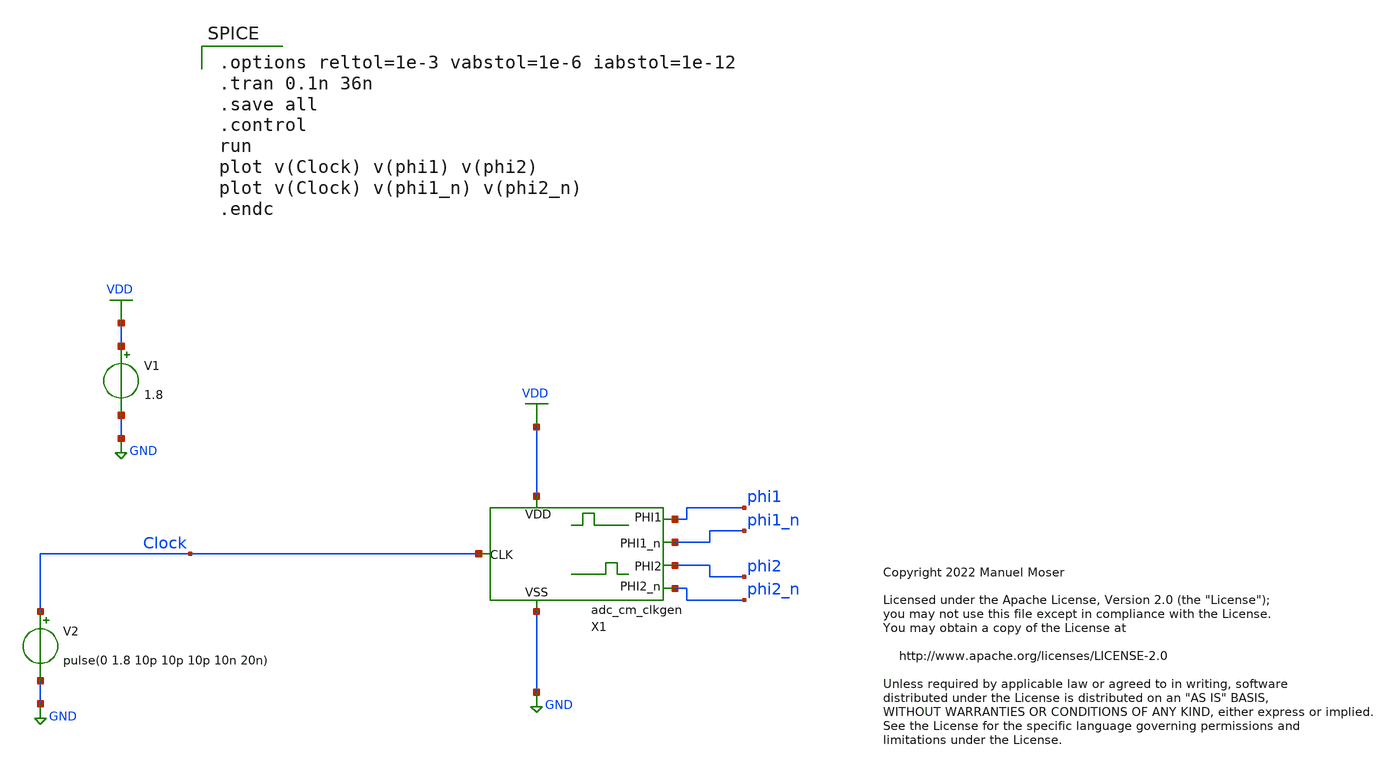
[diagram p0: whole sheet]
** sch_path: xschem/adc_cm_clkgen/adc_cm_clkgen_transient.sch
* Copyright 2022 Manuel Moser
* Licensed under the Apache License, Version 2.0 (the "License");
**.subckt adc_cm_clkgen_transient
V1 VDD GND 1.8
V2 Clock GND pulse(0 1.8 10p 10p 10p 10n 20n)
X1 Clock VDD GND phi1_n phi1 phi2 phi2_n adc_cm_clkgen
**** begin user architecture code

.options reltol=1e-3 vabstol=1e-6 iabstol=1e-12
.tran 0.1n 36n
.save all
.control
run
plot v(Clock) v(phi1) v(phi2)
plot v(Clock) v(phi1_n) v(phi2_n)
.endc



** opencircuitdesign pdks install
.lib $::SKYWATER_MODELS/sky130.lib.spice tt


**** end user architecture code
**.ends
.GLOBAL GND
.GLOBAL VDD
.end
